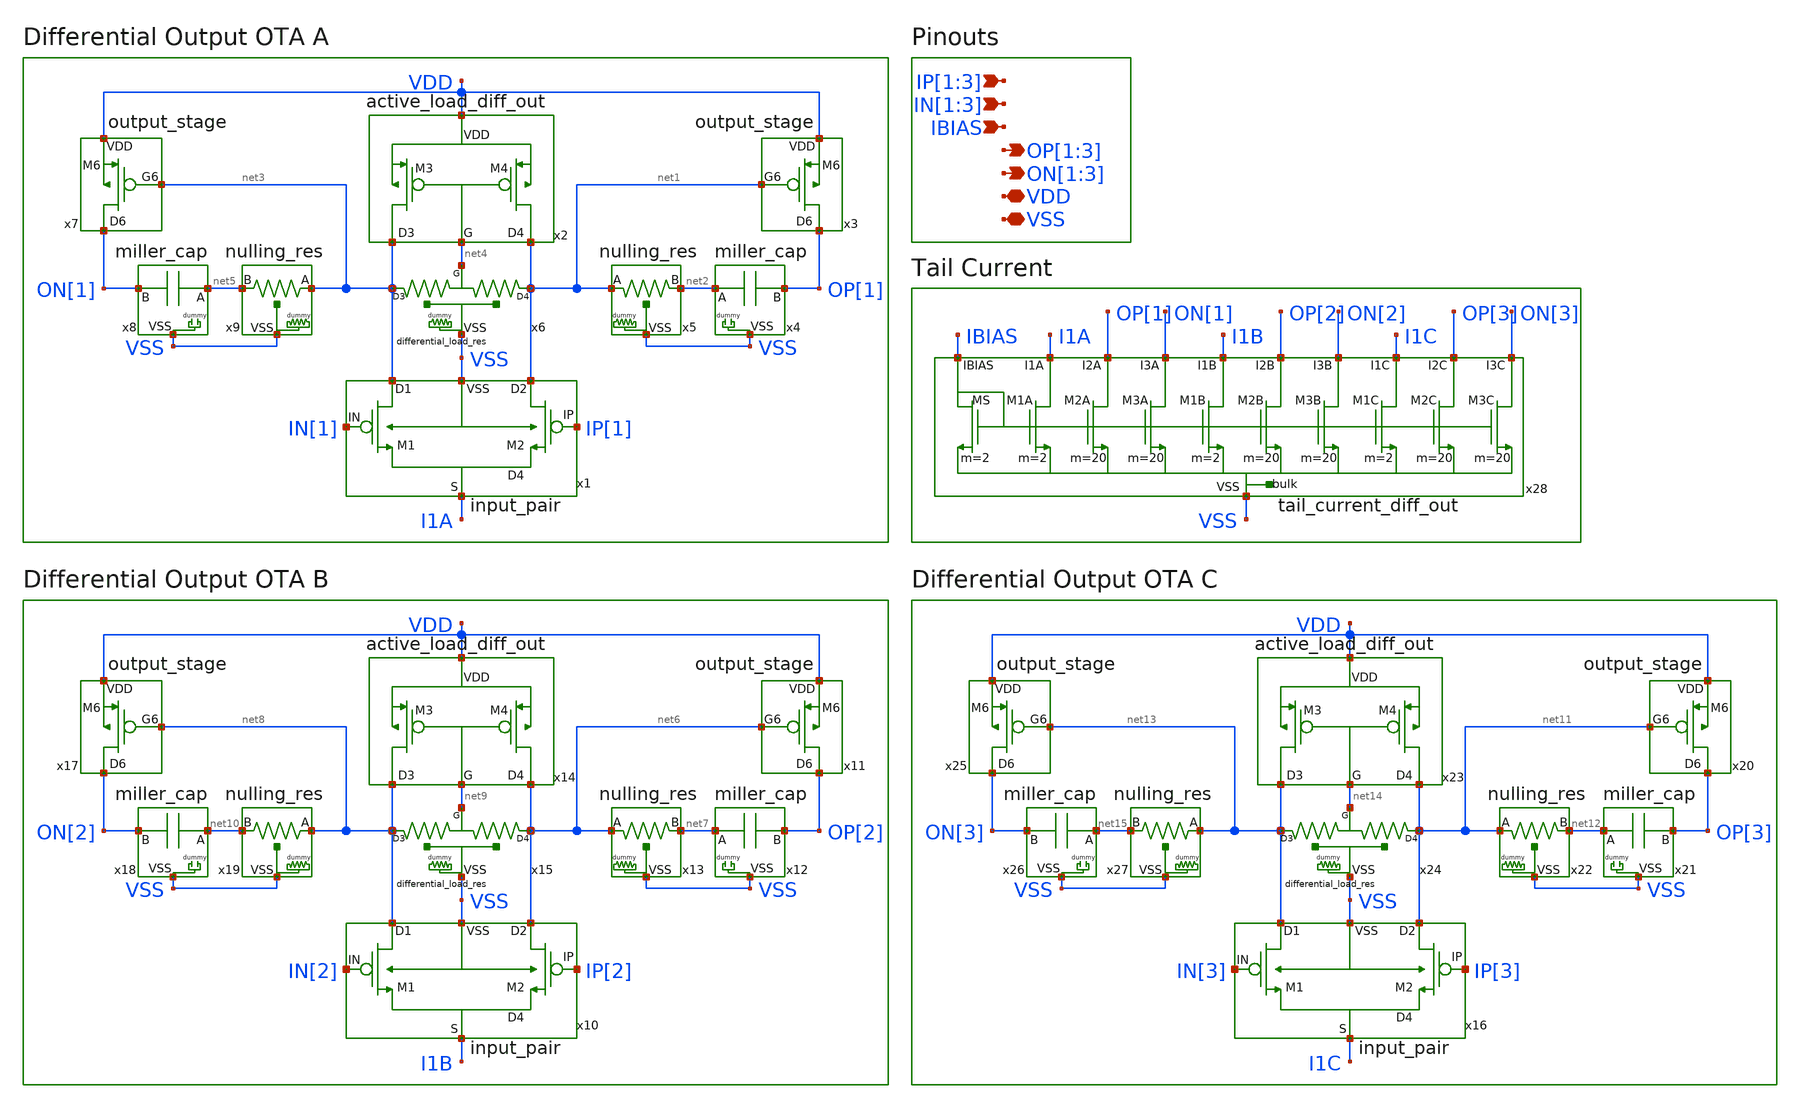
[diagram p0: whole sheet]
** sch_path: designs/libs/core_ota/three_differential_output_ota/three_differential_output_ota.sch
**.subckt three_differential_output_ota IP[1],IP[2],IP[3] IN[1],IN[2],IN[3] VDD VSS IBIAS
*+ OP[1],OP[2],OP[3] ON[1],ON[2],ON[3]
*.ipin IP[1],IP[2],IP[3]
*.ipin IN[1],IN[2],IN[3]
*.iopin VDD
*.iopin VSS
*.ipin IBIAS
*.opin OP[1],OP[2],OP[3]
*.opin ON[1],ON[2],ON[3]
x1 IN[1] IP[1] I1A net1 net3 VSS input_pair
x3 OP[1] VDD net1 output_stage
x4 net2 OP[1] VSS miller_cap
x5 net1 net2 VSS nulling_res
x2 net3 net1 VDD net4 active_load_diff_out
x6 net3 VSS net4 net1 differential_load_res
x7 ON[1] VDD net3 output_stage
x8 net5 ON[1] VSS miller_cap
x9 net3 net5 VSS nulling_res
x10 IN[2] IP[2] I1B net6 net8 VSS input_pair
x11 OP[2] VDD net6 output_stage
x12 net7 OP[2] VSS miller_cap
x13 net6 net7 VSS nulling_res
x14 net8 net6 VDD net9 active_load_diff_out
x15 net8 VSS net9 net6 differential_load_res
x17 ON[2] VDD net8 output_stage
x18 net10 ON[2] VSS miller_cap
x19 net8 net10 VSS nulling_res
x16 IN[3] IP[3] I1C net11 net13 VSS input_pair
x20 OP[3] VDD net11 output_stage
x21 net12 OP[3] VSS miller_cap
x22 net11 net12 VSS nulling_res
x23 net13 net11 VDD net14 active_load_diff_out
x24 net13 VSS net14 net11 differential_load_res
x25 ON[3] VDD net13 output_stage
x26 net15 ON[3] VSS miller_cap
x27 net13 net15 VSS nulling_res
x28 IBIAS I1A OP[1] ON[1] I1B OP[2] ON[2] I1C OP[3] ON[3] VSS tail_current_diff_out
**.ends
.end
